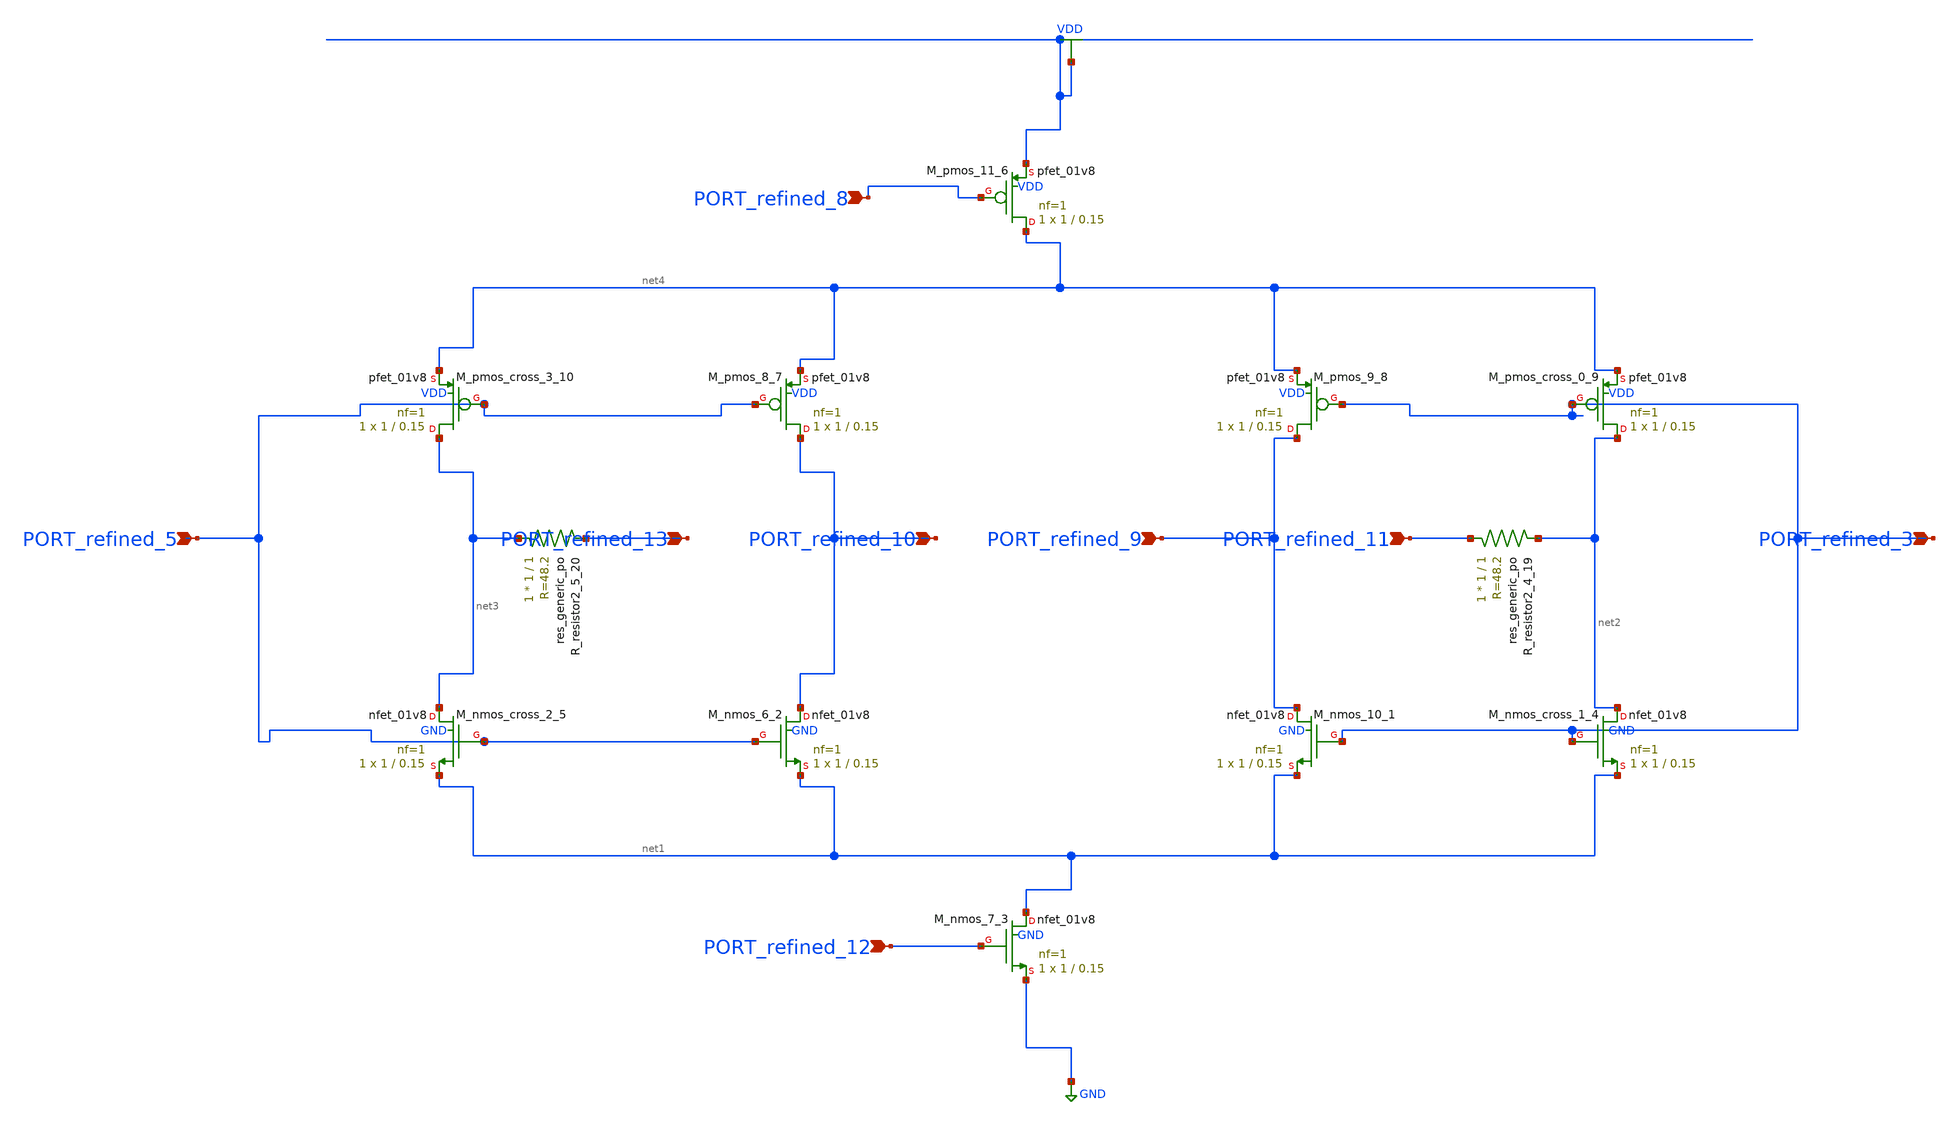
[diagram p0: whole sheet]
** sch_path: schematics/10_1109_ACCESS_2020_2989192_09_002.sch
**.subckt 10_1109_ACCESS_2020_2989192_09_002 PORT_refined_11 PORT_refined_10 PORT_refined_9
*+ PORT_refined_5 PORT_refined_3 PORT_refined_8 PORT_refined_12 PORT_refined_13
*.ipin PORT_refined_11
*.ipin PORT_refined_10
*.ipin PORT_refined_9
*.ipin PORT_refined_5
*.ipin PORT_refined_3
*.ipin PORT_refined_8
*.ipin PORT_refined_12
*.ipin PORT_refined_13
XM_nmos_10_1 PORT_refined_9 PORT_refined_3 net1 GND sky130_fd_pr__nfet_01v8 L=0.15 W=1 nf=1 ad='int((1 + 1)/2) * 1 / 1 * 0.29'
+ as='int((1 + 2)/2) * 1 / 1 * 0.29' pd='2*int((1 + 1)/2) * (1 / 1 + 0.29)' ps='2*int((1 + 2)/2) * (1 / 1 + 0.29)'
+ nrd='0.29 / 1 ' nrs='0.29 / 1 ' sa=0 sb=0 sd=0 mult=1 m=1
XM_nmos_6_2 PORT_refined_10 PORT_refined_5 net1 GND sky130_fd_pr__nfet_01v8 L=0.15 W=1 nf=1 ad='int((1 + 1)/2) * 1 / 1 * 0.29'
+ as='int((1 + 2)/2) * 1 / 1 * 0.29' pd='2*int((1 + 1)/2) * (1 / 1 + 0.29)' ps='2*int((1 + 2)/2) * (1 / 1 + 0.29)'
+ nrd='0.29 / 1 ' nrs='0.29 / 1 ' sa=0 sb=0 sd=0 mult=1 m=1
XM_nmos_7_3 net1 PORT_refined_12 GND GND sky130_fd_pr__nfet_01v8 L=0.15 W=1 nf=1 ad='int((1 + 1)/2) * 1 / 1 * 0.29'
+ as='int((1 + 2)/2) * 1 / 1 * 0.29' pd='2*int((1 + 1)/2) * (1 / 1 + 0.29)' ps='2*int((1 + 2)/2) * (1 / 1 + 0.29)'
+ nrd='0.29 / 1 ' nrs='0.29 / 1 ' sa=0 sb=0 sd=0 mult=1 m=1
XM_nmos_cross_1_4 net2 PORT_refined_3 net1 GND sky130_fd_pr__nfet_01v8 L=0.15 W=1 nf=1 ad='int((1 + 1)/2) * 1 / 1 * 0.29'
+ as='int((1 + 2)/2) * 1 / 1 * 0.29' pd='2*int((1 + 1)/2) * (1 / 1 + 0.29)' ps='2*int((1 + 2)/2) * (1 / 1 + 0.29)'
+ nrd='0.29 / 1 ' nrs='0.29 / 1 ' sa=0 sb=0 sd=0 mult=1 m=1
XM_nmos_cross_2_5 net3 PORT_refined_5 net1 GND sky130_fd_pr__nfet_01v8 L=0.15 W=1 nf=1 ad='int((1 + 1)/2) * 1 / 1 * 0.29'
+ as='int((1 + 2)/2) * 1 / 1 * 0.29' pd='2*int((1 + 1)/2) * (1 / 1 + 0.29)' ps='2*int((1 + 2)/2) * (1 / 1 + 0.29)'
+ nrd='0.29 / 1 ' nrs='0.29 / 1 ' sa=0 sb=0 sd=0 mult=1 m=1
XM_pmos_11_6 net4 PORT_refined_8 VDD VDD sky130_fd_pr__pfet_01v8 L=0.15 W=1 nf=1 ad='int((1 + 1)/2) * 1 / 1 * 0.29'
+ as='int((1 + 2)/2) * 1 / 1 * 0.29' pd='2*int((1 + 1)/2) * (1 / 1 + 0.29)' ps='2*int((1 + 2)/2) * (1 / 1 + 0.29)'
+ nrd='0.29 / 1 ' nrs='0.29 / 1 ' sa=0 sb=0 sd=0 mult=1 m=1
XM_pmos_8_7 PORT_refined_10 PORT_refined_5 net4 VDD sky130_fd_pr__pfet_01v8 L=0.15 W=1 nf=1 ad='int((1 + 1)/2) * 1 / 1 * 0.29'
+ as='int((1 + 2)/2) * 1 / 1 * 0.29' pd='2*int((1 + 1)/2) * (1 / 1 + 0.29)' ps='2*int((1 + 2)/2) * (1 / 1 + 0.29)'
+ nrd='0.29 / 1 ' nrs='0.29 / 1 ' sa=0 sb=0 sd=0 mult=1 m=1
XM_pmos_9_8 PORT_refined_9 PORT_refined_3 net4 VDD sky130_fd_pr__pfet_01v8 L=0.15 W=1 nf=1 ad='int((1 + 1)/2) * 1 / 1 * 0.29'
+ as='int((1 + 2)/2) * 1 / 1 * 0.29' pd='2*int((1 + 1)/2) * (1 / 1 + 0.29)' ps='2*int((1 + 2)/2) * (1 / 1 + 0.29)'
+ nrd='0.29 / 1 ' nrs='0.29 / 1 ' sa=0 sb=0 sd=0 mult=1 m=1
XM_pmos_cross_0_9 net2 PORT_refined_3 net4 VDD sky130_fd_pr__pfet_01v8 L=0.15 W=1 nf=1 ad='int((1 + 1)/2) * 1 / 1 * 0.29'
+ as='int((1 + 2)/2) * 1 / 1 * 0.29' pd='2*int((1 + 1)/2) * (1 / 1 + 0.29)' ps='2*int((1 + 2)/2) * (1 / 1 + 0.29)'
+ nrd='0.29 / 1 ' nrs='0.29 / 1 ' sa=0 sb=0 sd=0 mult=1 m=1
XM_pmos_cross_3_10 net3 PORT_refined_5 net4 VDD sky130_fd_pr__pfet_01v8 L=0.15 W=1 nf=1 ad='int((1 + 1)/2) * 1 / 1 * 0.29'
+ as='int((1 + 2)/2) * 1 / 1 * 0.29' pd='2*int((1 + 1)/2) * (1 / 1 + 0.29)' ps='2*int((1 + 2)/2) * (1 / 1 + 0.29)'
+ nrd='0.29 / 1 ' nrs='0.29 / 1 ' sa=0 sb=0 sd=0 mult=1 m=1
XR_resistor2_4_19 PORT_refined_11 net2 sky130_fd_pr__res_generic_po W=1 L=1 m=1
XR_resistor2_5_20 net3 PORT_refined_13 sky130_fd_pr__res_generic_po W=1 L=1 m=1
**.ends
.GLOBAL GND
.GLOBAL VDD
.end
